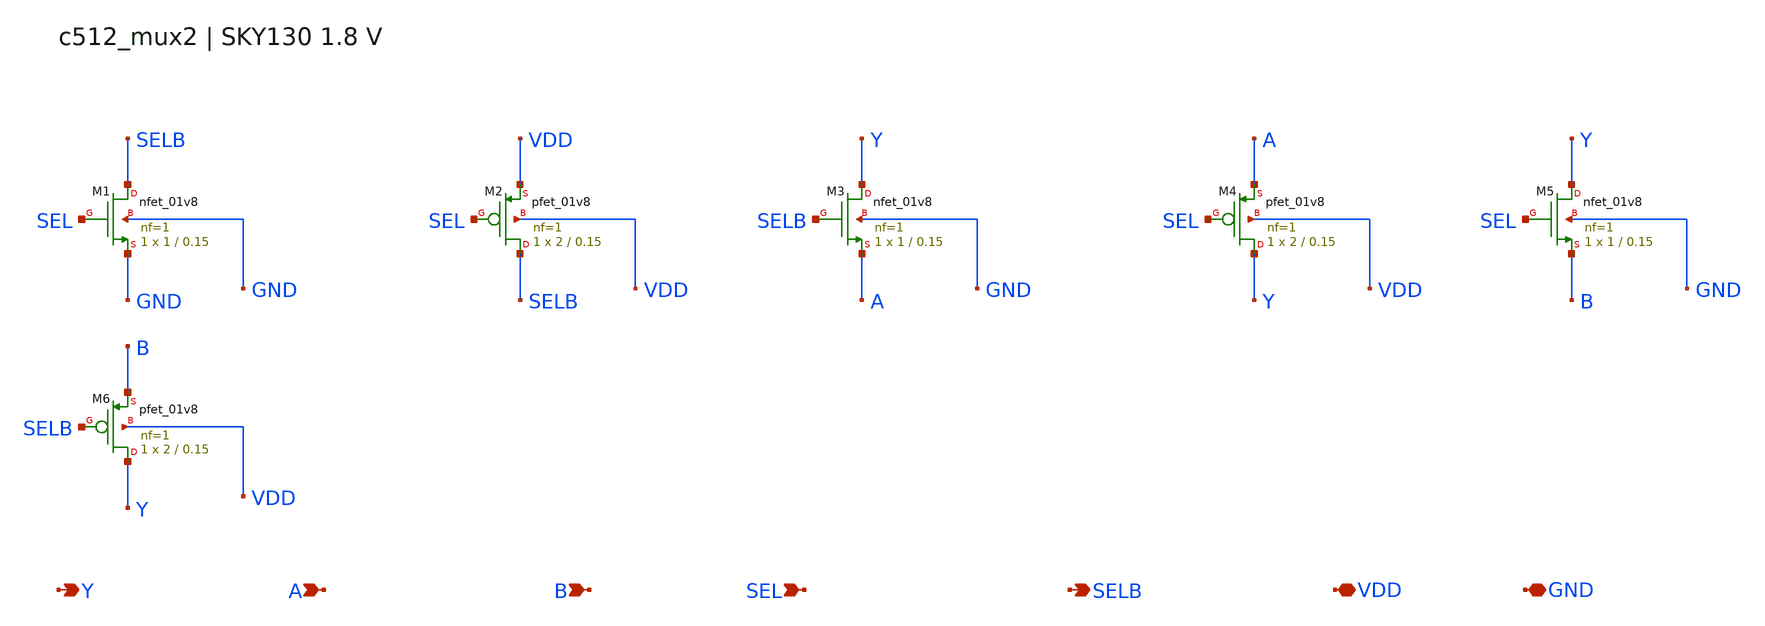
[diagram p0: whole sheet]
** sch_path: c512_mux2.sch
**.subckt c512_mux2 Y A B SEL SELB VDD GND
*.opin Y
*.ipin A
*.ipin B
*.ipin SEL
*.opin SELB
*.iopin VDD
*.iopin GND
XM1 SELB SEL GND GND sky130_fd_pr__nfet_01v8 L=0.15 W=1 nf=1 ad=0.29 as=0.29 pd=2.58 ps=2.58
+ nrd=0.29 nrs=0.29 sa=0 sb=0 sd=0 mult=1 m=1
XM2 SELB SEL VDD VDD sky130_fd_pr__pfet_01v8 L=0.15 W=2 nf=1 ad=0.58 as=0.58 pd=4.58 ps=4.58
+ nrd=0.145 nrs=0.145 sa=0 sb=0 sd=0 mult=1 m=1
XM3 Y SELB A GND sky130_fd_pr__nfet_01v8 L=0.15 W=1 nf=1 ad=0.29 as=0.29 pd=2.58 ps=2.58 nrd=0.29
+ nrs=0.29 sa=0 sb=0 sd=0 mult=1 m=1
XM4 Y SEL A VDD sky130_fd_pr__pfet_01v8 L=0.15 W=2 nf=1 ad=0.58 as=0.58 pd=4.58 ps=4.58 nrd=0.145
+ nrs=0.145 sa=0 sb=0 sd=0 mult=1 m=1
XM5 Y SEL B GND sky130_fd_pr__nfet_01v8 L=0.15 W=1 nf=1 ad=0.29 as=0.29 pd=2.58 ps=2.58 nrd=0.29
+ nrs=0.29 sa=0 sb=0 sd=0 mult=1 m=1
XM6 Y SELB B VDD sky130_fd_pr__pfet_01v8 L=0.15 W=2 nf=1 ad=0.58 as=0.58 pd=4.58 ps=4.58 nrd=0.145
+ nrs=0.145 sa=0 sb=0 sd=0 mult=1 m=1
**.ends
.end
